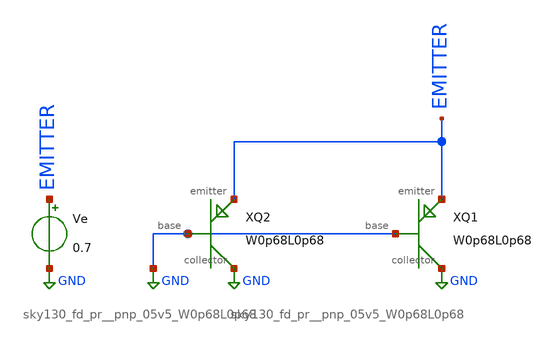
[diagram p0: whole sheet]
** sch_path: projects/pnp/xschem_ngspice/tb_pnp.sch
**.subckt tb_pnp
Ve EMITTER GND 0.7
XQ1 EMITTER GND GND sky130_fd_pr__pnp_05v5_W0p68L0p68
XQ2 EMITTER GND GND sky130_fd_pr__pnp_05v5_W0p68L0p68
**** begin user architecture code



.lib /foss/pdks/sky130A/libs.tech/ngspice/sky130.lib.spice tt

.subckt sky130_fd_pr__pnp_05v5_W0p68L0p68.model emitter base collector
.include /foss/pdks/volare/sky130/versions/bdc9412b3e468c102d01b7cf6337be06ec6e9c9a/sky130A/libs.ref/sky130_fd_pr/spice/sky130_fd_pr__pnp_05v5_W0p68L0p68.model.spice
.ends

.control
dc ve 0.3 0.8 0.001
plot i(ve)
.endc



**** end user architecture code
**.ends
.GLOBAL GND
.end
